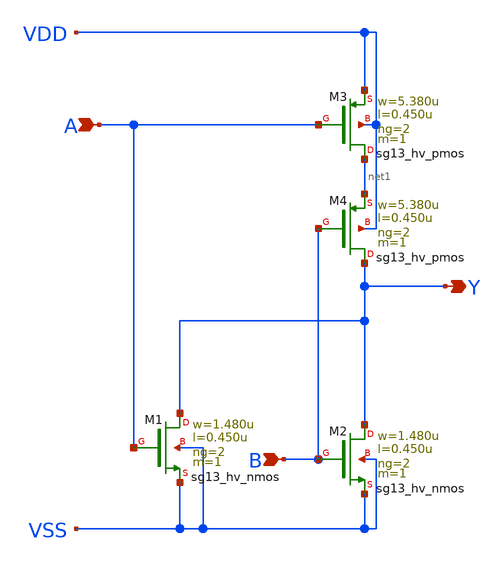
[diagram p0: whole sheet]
** sch_path: ihp-sg13g2/libs.ref/sg13g2_stdcell_hv/sch/xschem/sg13g2_hv_nor2_2.sch
* Copyright 2023 IHP PDK Authors
* Licensed under the Apache License, Version 2.0 (the "License");
* you may not use this file except in compliance with the License.
* You may obtain a copy of the License at
* https://www.apache.org/licenses/LICENSE-2.0
* Unless required by applicable law or agreed to in writing, software
* distributed under the License is distributed on an "AS IS" BASIS,
* WITHOUT WARRANTIES OR CONDITIONS OF ANY KIND, either express or implied.
* See the License for the specific language governing permissions and
* limitations under the License.
**.subckt sg13g2_hv_nor2_2 Y B A
*.opin Y
*.ipin B
*.ipin A
XM1 Y A VSS VSS sg13_hv_nmos w=1.480u l=0.450u ng=2 m=1 mm_ok=1
XM2 Y B VSS VSS sg13_hv_nmos w=1.480u l=0.450u ng=2 m=1 mm_ok=1
XM3 net1 A VDD VDD sg13_hv_pmos w=5.380u l=0.450u ng=2 m=1 mm_ok=1
XM4 Y B net1 VDD sg13_hv_pmos w=5.380u l=0.450u ng=2 m=1 mm_ok=1
**.ends
.end
